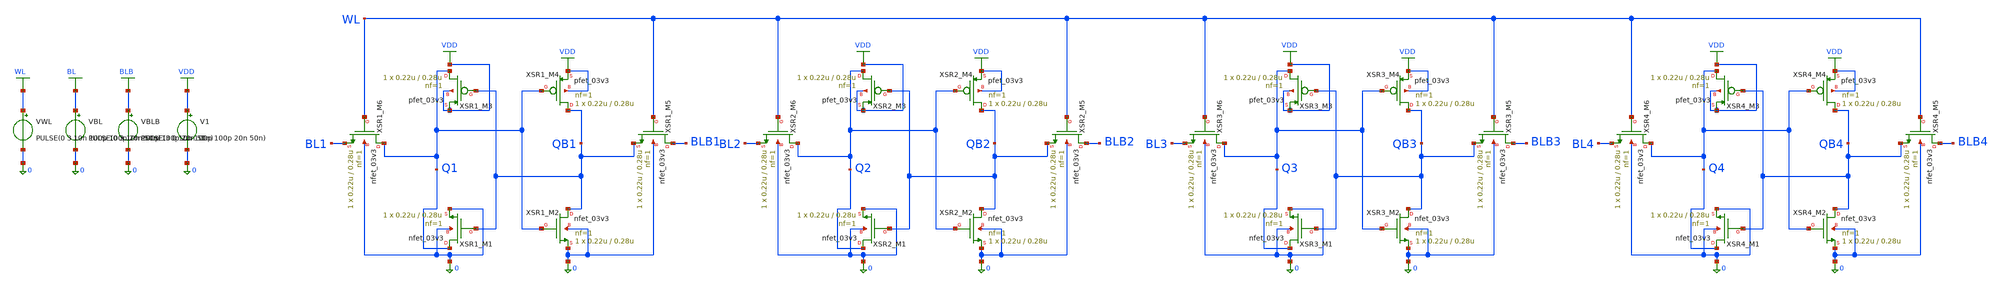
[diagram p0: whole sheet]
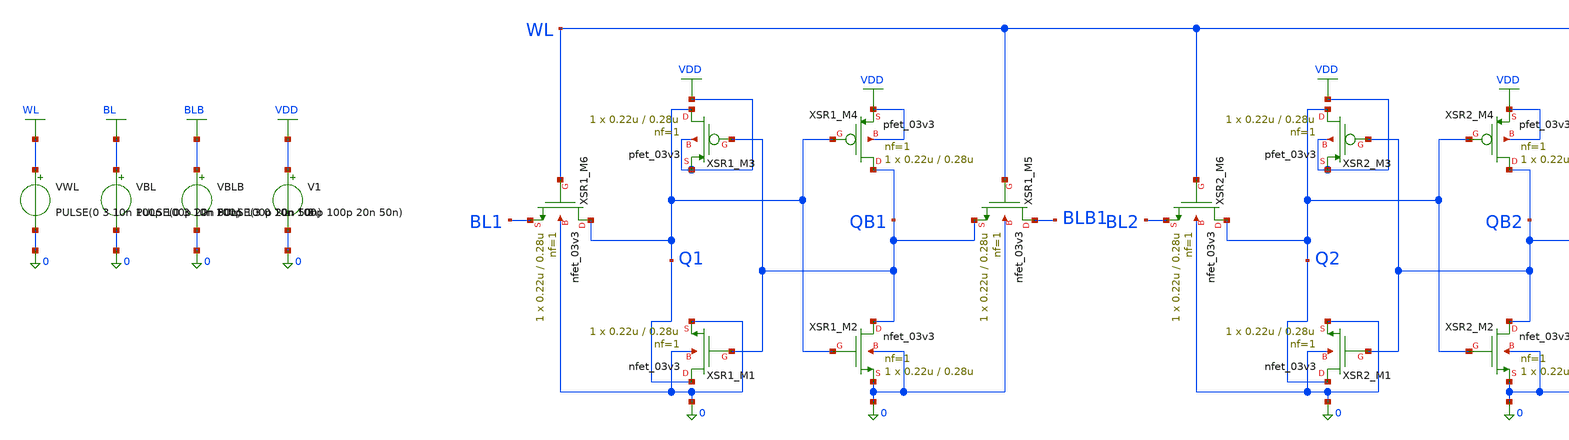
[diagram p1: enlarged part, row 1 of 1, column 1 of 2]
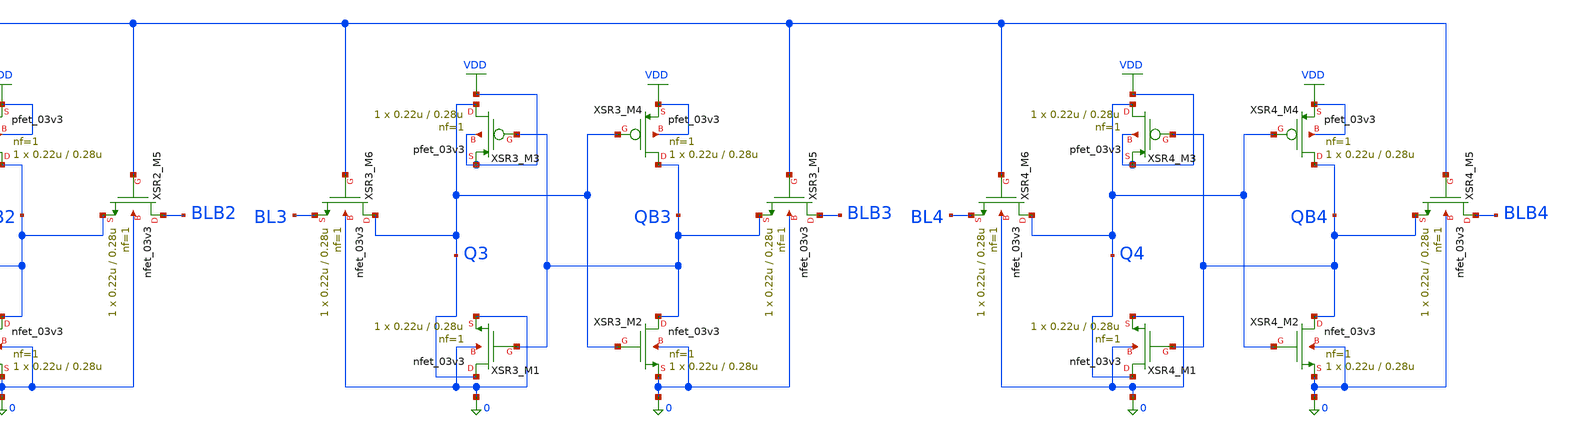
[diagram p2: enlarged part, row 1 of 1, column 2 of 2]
** sch_path: src/schematic/SRAM_6T/sram_6t.sch
**.subckt sram_6t
XSR1_M6 Q1 WL BL1 0 nfet_03v3 L=0.28u W=0.22u nf=1 ad='int((nf+1)/2) * W/nf * 0.18u' as='int((nf+2)/2) * W/nf * 0.18u'
+ pd='2*int((nf+1)/2) * (W/nf + 0.18u)' ps='2*int((nf+2)/2) * (W/nf + 0.18u)' nrd='0.18u / W' nrs='0.18u / W'
+ sa=0 sb=0 sd=0 m=1
XSR1_M3 Q1 QB1 VDD VDD pfet_03v3 L=0.28u W=0.22u nf=1 ad='int((nf+1)/2) * W/nf * 0.18u' as='int((nf+2)/2) * W/nf * 0.18u'
+ pd='2*int((nf+1)/2) * (W/nf + 0.18u)' ps='2*int((nf+2)/2) * (W/nf + 0.18u)' nrd='0.18u / W' nrs='0.18u / W'
+ sa=0 sb=0 sd=0 m=1
XSR1_M4 QB1 Q1 VDD VDD pfet_03v3 L=0.28u W=0.22u nf=1 ad='int((nf+1)/2) * W/nf * 0.18u' as='int((nf+2)/2) * W/nf * 0.18u'
+ pd='2*int((nf+1)/2) * (W/nf + 0.18u)' ps='2*int((nf+2)/2) * (W/nf + 0.18u)' nrd='0.18u / W' nrs='0.18u / W'
+ sa=0 sb=0 sd=0 m=1
XSR1_M5 BLB1 WL QB1 0 nfet_03v3 L=0.28u W=0.22u nf=1 ad='int((nf+1)/2) * W/nf * 0.18u' as='int((nf+2)/2) * W/nf * 0.18u'
+ pd='2*int((nf+1)/2) * (W/nf + 0.18u)' ps='2*int((nf+2)/2) * (W/nf + 0.18u)' nrd='0.18u / W' nrs='0.18u / W'
+ sa=0 sb=0 sd=0 m=1
XSR1_M1 Q1 QB1 0 0 nfet_03v3 L=0.28u W=0.22u nf=1 ad='int((nf+1)/2) * W/nf * 0.18u' as='int((nf+2)/2) * W/nf * 0.18u'
+ pd='2*int((nf+1)/2) * (W/nf + 0.18u)' ps='2*int((nf+2)/2) * (W/nf + 0.18u)' nrd='0.18u / W' nrs='0.18u / W'
+ sa=0 sb=0 sd=0 m=1
XSR1_M2 QB1 Q1 0 0 nfet_03v3 L=0.28u W=0.22u nf=1 ad='int((nf+1)/2) * W/nf * 0.18u' as='int((nf+2)/2) * W/nf * 0.18u'
+ pd='2*int((nf+1)/2) * (W/nf + 0.18u)' ps='2*int((nf+2)/2) * (W/nf + 0.18u)' nrd='0.18u / W' nrs='0.18u / W'
+ sa=0 sb=0 sd=0 m=1
V1 VDD 0 3
VBLB BLB 0 PULSE(3 0 10n 100p 100p 20n 50n)
VBL BL 0 PULSE(0 3 10n 100p 100p 20n 50n)
VWL WL 0 PULSE(0 3 10n 100p 100p 20n 50n)
XSR2_M6 Q2 WL BL2 0 nfet_03v3 L=0.28u W=0.22u nf=1 ad='int((nf+1)/2) * W/nf * 0.18u' as='int((nf+2)/2) * W/nf * 0.18u'
+ pd='2*int((nf+1)/2) * (W/nf + 0.18u)' ps='2*int((nf+2)/2) * (W/nf + 0.18u)' nrd='0.18u / W' nrs='0.18u / W'
+ sa=0 sb=0 sd=0 m=1
XSR2_M3 Q2 QB2 VDD VDD pfet_03v3 L=0.28u W=0.22u nf=1 ad='int((nf+1)/2) * W/nf * 0.18u' as='int((nf+2)/2) * W/nf * 0.18u'
+ pd='2*int((nf+1)/2) * (W/nf + 0.18u)' ps='2*int((nf+2)/2) * (W/nf + 0.18u)' nrd='0.18u / W' nrs='0.18u / W'
+ sa=0 sb=0 sd=0 m=1
XSR2_M4 QB2 Q2 VDD VDD pfet_03v3 L=0.28u W=0.22u nf=1 ad='int((nf+1)/2) * W/nf * 0.18u' as='int((nf+2)/2) * W/nf * 0.18u'
+ pd='2*int((nf+1)/2) * (W/nf + 0.18u)' ps='2*int((nf+2)/2) * (W/nf + 0.18u)' nrd='0.18u / W' nrs='0.18u / W'
+ sa=0 sb=0 sd=0 m=1
XSR2_M5 BLB2 WL QB2 0 nfet_03v3 L=0.28u W=0.22u nf=1 ad='int((nf+1)/2) * W/nf * 0.18u' as='int((nf+2)/2) * W/nf * 0.18u'
+ pd='2*int((nf+1)/2) * (W/nf + 0.18u)' ps='2*int((nf+2)/2) * (W/nf + 0.18u)' nrd='0.18u / W' nrs='0.18u / W'
+ sa=0 sb=0 sd=0 m=1
XSR2_M1 Q2 QB2 0 0 nfet_03v3 L=0.28u W=0.22u nf=1 ad='int((nf+1)/2) * W/nf * 0.18u' as='int((nf+2)/2) * W/nf * 0.18u'
+ pd='2*int((nf+1)/2) * (W/nf + 0.18u)' ps='2*int((nf+2)/2) * (W/nf + 0.18u)' nrd='0.18u / W' nrs='0.18u / W'
+ sa=0 sb=0 sd=0 m=1
XSR2_M2 QB2 Q2 0 0 nfet_03v3 L=0.28u W=0.22u nf=1 ad='int((nf+1)/2) * W/nf * 0.18u' as='int((nf+2)/2) * W/nf * 0.18u'
+ pd='2*int((nf+1)/2) * (W/nf + 0.18u)' ps='2*int((nf+2)/2) * (W/nf + 0.18u)' nrd='0.18u / W' nrs='0.18u / W'
+ sa=0 sb=0 sd=0 m=1
XSR3_M6 Q3 WL BL3 0 nfet_03v3 L=0.28u W=0.22u nf=1 ad='int((nf+1)/2) * W/nf * 0.18u' as='int((nf+2)/2) * W/nf * 0.18u'
+ pd='2*int((nf+1)/2) * (W/nf + 0.18u)' ps='2*int((nf+2)/2) * (W/nf + 0.18u)' nrd='0.18u / W' nrs='0.18u / W'
+ sa=0 sb=0 sd=0 m=1
XSR3_M3 Q3 QB3 VDD VDD pfet_03v3 L=0.28u W=0.22u nf=1 ad='int((nf+1)/2) * W/nf * 0.18u' as='int((nf+2)/2) * W/nf * 0.18u'
+ pd='2*int((nf+1)/2) * (W/nf + 0.18u)' ps='2*int((nf+2)/2) * (W/nf + 0.18u)' nrd='0.18u / W' nrs='0.18u / W'
+ sa=0 sb=0 sd=0 m=1
XSR3_M4 QB3 Q3 VDD VDD pfet_03v3 L=0.28u W=0.22u nf=1 ad='int((nf+1)/2) * W/nf * 0.18u' as='int((nf+2)/2) * W/nf * 0.18u'
+ pd='2*int((nf+1)/2) * (W/nf + 0.18u)' ps='2*int((nf+2)/2) * (W/nf + 0.18u)' nrd='0.18u / W' nrs='0.18u / W'
+ sa=0 sb=0 sd=0 m=1
XSR3_M5 BLB3 WL QB3 0 nfet_03v3 L=0.28u W=0.22u nf=1 ad='int((nf+1)/2) * W/nf * 0.18u' as='int((nf+2)/2) * W/nf * 0.18u'
+ pd='2*int((nf+1)/2) * (W/nf + 0.18u)' ps='2*int((nf+2)/2) * (W/nf + 0.18u)' nrd='0.18u / W' nrs='0.18u / W'
+ sa=0 sb=0 sd=0 m=1
XSR3_M1 Q3 QB3 0 0 nfet_03v3 L=0.28u W=0.22u nf=1 ad='int((nf+1)/2) * W/nf * 0.18u' as='int((nf+2)/2) * W/nf * 0.18u'
+ pd='2*int((nf+1)/2) * (W/nf + 0.18u)' ps='2*int((nf+2)/2) * (W/nf + 0.18u)' nrd='0.18u / W' nrs='0.18u / W'
+ sa=0 sb=0 sd=0 m=1
XSR3_M2 QB3 Q3 0 0 nfet_03v3 L=0.28u W=0.22u nf=1 ad='int((nf+1)/2) * W/nf * 0.18u' as='int((nf+2)/2) * W/nf * 0.18u'
+ pd='2*int((nf+1)/2) * (W/nf + 0.18u)' ps='2*int((nf+2)/2) * (W/nf + 0.18u)' nrd='0.18u / W' nrs='0.18u / W'
+ sa=0 sb=0 sd=0 m=1
XSR4_M6 Q4 WL BL4 0 nfet_03v3 L=0.28u W=0.22u nf=1 ad='int((nf+1)/2) * W/nf * 0.18u' as='int((nf+2)/2) * W/nf * 0.18u'
+ pd='2*int((nf+1)/2) * (W/nf + 0.18u)' ps='2*int((nf+2)/2) * (W/nf + 0.18u)' nrd='0.18u / W' nrs='0.18u / W'
+ sa=0 sb=0 sd=0 m=1
XSR4_M3 Q4 QB4 VDD VDD pfet_03v3 L=0.28u W=0.22u nf=1 ad='int((nf+1)/2) * W/nf * 0.18u' as='int((nf+2)/2) * W/nf * 0.18u'
+ pd='2*int((nf+1)/2) * (W/nf + 0.18u)' ps='2*int((nf+2)/2) * (W/nf + 0.18u)' nrd='0.18u / W' nrs='0.18u / W'
+ sa=0 sb=0 sd=0 m=1
XSR4_M4 QB4 Q4 VDD VDD pfet_03v3 L=0.28u W=0.22u nf=1 ad='int((nf+1)/2) * W/nf * 0.18u' as='int((nf+2)/2) * W/nf * 0.18u'
+ pd='2*int((nf+1)/2) * (W/nf + 0.18u)' ps='2*int((nf+2)/2) * (W/nf + 0.18u)' nrd='0.18u / W' nrs='0.18u / W'
+ sa=0 sb=0 sd=0 m=1
XSR4_M5 BLB4 WL QB4 0 nfet_03v3 L=0.28u W=0.22u nf=1 ad='int((nf+1)/2) * W/nf * 0.18u' as='int((nf+2)/2) * W/nf * 0.18u'
+ pd='2*int((nf+1)/2) * (W/nf + 0.18u)' ps='2*int((nf+2)/2) * (W/nf + 0.18u)' nrd='0.18u / W' nrs='0.18u / W'
+ sa=0 sb=0 sd=0 m=1
XSR4_M1 Q4 QB4 0 0 nfet_03v3 L=0.28u W=0.22u nf=1 ad='int((nf+1)/2) * W/nf * 0.18u' as='int((nf+2)/2) * W/nf * 0.18u'
+ pd='2*int((nf+1)/2) * (W/nf + 0.18u)' ps='2*int((nf+2)/2) * (W/nf + 0.18u)' nrd='0.18u / W' nrs='0.18u / W'
+ sa=0 sb=0 sd=0 m=1
XSR4_M2 QB4 Q4 0 0 nfet_03v3 L=0.28u W=0.22u nf=1 ad='int((nf+1)/2) * W/nf * 0.18u' as='int((nf+2)/2) * W/nf * 0.18u'
+ pd='2*int((nf+1)/2) * (W/nf + 0.18u)' ps='2*int((nf+2)/2) * (W/nf + 0.18u)' nrd='0.18u / W' nrs='0.18u / W'
+ sa=0 sb=0 sd=0 m=1
**** begin user architecture code


.include /home/ziaalby/chipathon-2026-gf180mcu-padring/gf180mcu/gf180mcuD/libs.tech/ngspice/design.ngspice
.lib /home/ziaalby/chipathon-2026-gf180mcu-padring/gf180mcu/gf180mcuD/libs.tech/ngspice/sm141064.ngspice typical
.control
save all
tran 100p 100n
print v(q) v(qb) v(bl) v(blb) v(wl)
.endc


**** end user architecture code
**.ends
.GLOBAL VDD
.GLOBAL BLB
.GLOBAL BL
.GLOBAL WL
.end
